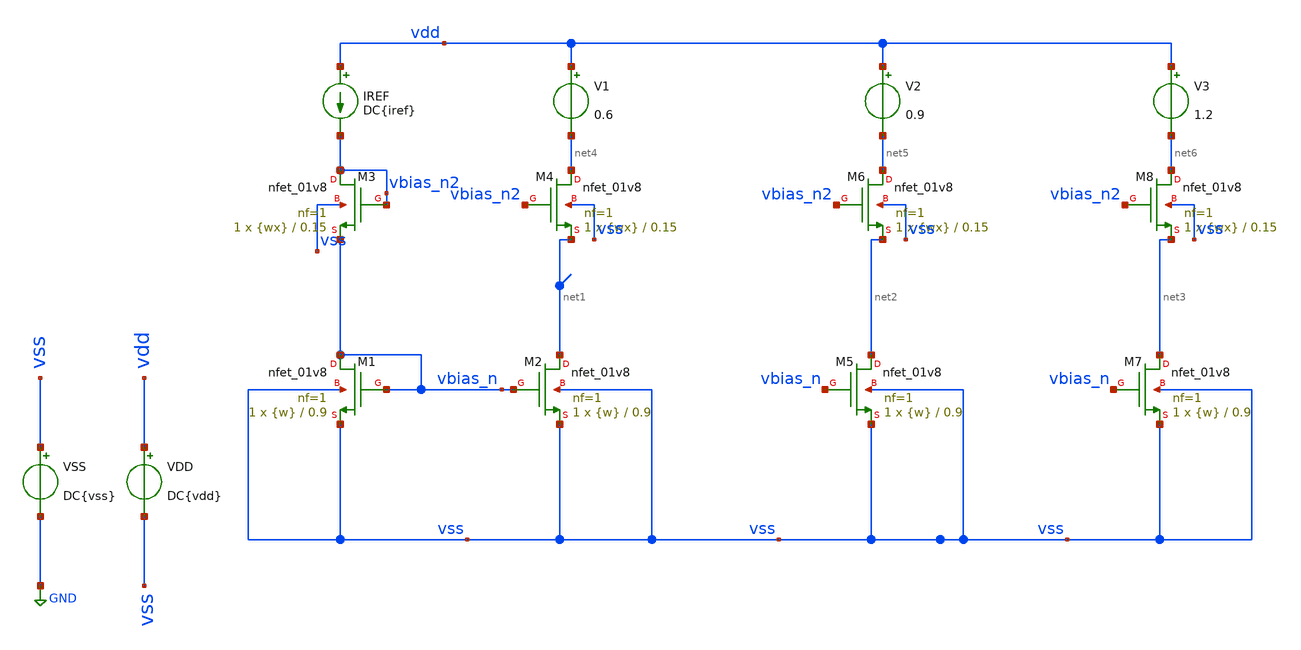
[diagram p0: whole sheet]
** sch_path: tp2/tp2_3.sch
**.subckt tp2_3
XM1 vbias_n vbias_n vss vss sky130_fd_pr__nfet_01v8 L=0.9 W={w} nf=1 ad='int((nf+1)/2) * W/nf * 0.29'
+ as='int((nf+2)/2) * W/nf * 0.29' pd='2*int((nf+1)/2) * (W/nf + 0.29)' ps='2*int((nf+2)/2) * (W/nf + 0.29)'
+ nrd='0.29 / W' nrs='0.29 / W' sa=0 sb=0 sd=0 mult=1 m=1
XM2 net1 vbias_n vss vss sky130_fd_pr__nfet_01v8 L=0.9 W={w} nf=1 ad='int((nf+1)/2) * W/nf * 0.29' as='int((nf+2)/2) * W/nf * 0.29'
+ pd='2*int((nf+1)/2) * (W/nf + 0.29)' ps='2*int((nf+2)/2) * (W/nf + 0.29)' nrd='0.29 / W' nrs='0.29 / W'
+ sa=0 sb=0 sd=0 mult=1 m=1
IREF vdd vbias_n2 DC{iref}
VSS vss GND DC{vss}
VDD vdd vss DC{vdd}
XM3 vbias_n2 vbias_n2 vbias_n vss sky130_fd_pr__nfet_01v8 L=0.15 W={wx} nf=1 ad='int((nf+1)/2) * W/nf * 0.29'
+ as='int((nf+2)/2) * W/nf * 0.29' pd='2*int((nf+1)/2) * (W/nf + 0.29)' ps='2*int((nf+2)/2) * (W/nf + 0.29)'
+ nrd='0.29 / W' nrs='0.29 / W' sa=0 sb=0 sd=0 mult=1 m=1
XM4 net4 vbias_n2 net1 vss sky130_fd_pr__nfet_01v8 L=0.15 W={wx} nf=1 ad='int((nf+1)/2) * W/nf * 0.29'
+ as='int((nf+2)/2) * W/nf * 0.29' pd='2*int((nf+1)/2) * (W/nf + 0.29)' ps='2*int((nf+2)/2) * (W/nf + 0.29)'
+ nrd='0.29 / W' nrs='0.29 / W' sa=0 sb=0 sd=0 mult=1 m=1
XM5 net2 vbias_n vss vss sky130_fd_pr__nfet_01v8 L=0.9 W={w} nf=1 ad='int((nf+1)/2) * W/nf * 0.29' as='int((nf+2)/2) * W/nf * 0.29'
+ pd='2*int((nf+1)/2) * (W/nf + 0.29)' ps='2*int((nf+2)/2) * (W/nf + 0.29)' nrd='0.29 / W' nrs='0.29 / W'
+ sa=0 sb=0 sd=0 mult=1 m=1
XM6 net5 vbias_n2 net2 vss sky130_fd_pr__nfet_01v8 L=0.15 W={wx} nf=1 ad='int((nf+1)/2) * W/nf * 0.29'
+ as='int((nf+2)/2) * W/nf * 0.29' pd='2*int((nf+1)/2) * (W/nf + 0.29)' ps='2*int((nf+2)/2) * (W/nf + 0.29)'
+ nrd='0.29 / W' nrs='0.29 / W' sa=0 sb=0 sd=0 mult=1 m=1
XM7 net3 vbias_n vss vss sky130_fd_pr__nfet_01v8 L=0.9 W={w} nf=1 ad='int((nf+1)/2) * W/nf * 0.29' as='int((nf+2)/2) * W/nf * 0.29'
+ pd='2*int((nf+1)/2) * (W/nf + 0.29)' ps='2*int((nf+2)/2) * (W/nf + 0.29)' nrd='0.29 / W' nrs='0.29 / W'
+ sa=0 sb=0 sd=0 mult=1 m=1
XM8 net6 vbias_n2 net3 vss sky130_fd_pr__nfet_01v8 L=0.15 W={wx} nf=1 ad='int((nf+1)/2) * W/nf * 0.29'
+ as='int((nf+2)/2) * W/nf * 0.29' pd='2*int((nf+1)/2) * (W/nf + 0.29)' ps='2*int((nf+2)/2) * (W/nf + 0.29)'
+ nrd='0.29 / W' nrs='0.29 / W' sa=0 sb=0 sd=0 mult=1 m=1
V1 vdd net4 0.6
V2 vdd net5 0.9
V3 vdd net6 1.2
**** begin user architecture code



* Parameters
.param vdd = 1.8
.param vss = 0.0
.param iref = 200u
.param w = 24
.param wx = 5
.param R = 4.5k
.options TEMPS = 27.0

* Models
*.lib ~/skywater/skywater-pdk/libraries/sky130_fd_pr_ngspice/latest/models/corners/sky130.lib TT
.lib /foss/pdks/sky130A/libs.tech/ngspice/sky130.lib.spice ff
* Data to save
.save all  @M.XM1.msky130_fd_pr__nfet_01v8[id]  @M.XM1.msky130_fd_pr__nfet_01v8[gm]  @M.XM1.msky130_fd_pr__nfet_01v8[vds]  @M.XM1.msky130_fd_pr__nfet_01v8[vgs]  @M.XM1.msky130_fd_pr__nfet_01v8[w]  @M.XM1.msky130_fd_pr__nfet_01v8[vth]  @M.XM2.msky130_fd_pr__nfet_01v8[id]  @M.XM2.msky130_fd_pr__nfet_01v8[gm]  @M.XM2.msky130_fd_pr__nfet_01v8[vds]  @M.XM2.msky130_fd_pr__nfet_01v8[vgs]  @M.XM2.msky130_fd_pr__nfet_01v8[w]  @M.XM2.msky130_fd_pr__nfet_01v8[vth]

* Simulation
.control

  op
  save all
  unset filetype
  write tp2_3.raw

.endc

.end


**** end user architecture code
**.ends
.GLOBAL GND
.end
